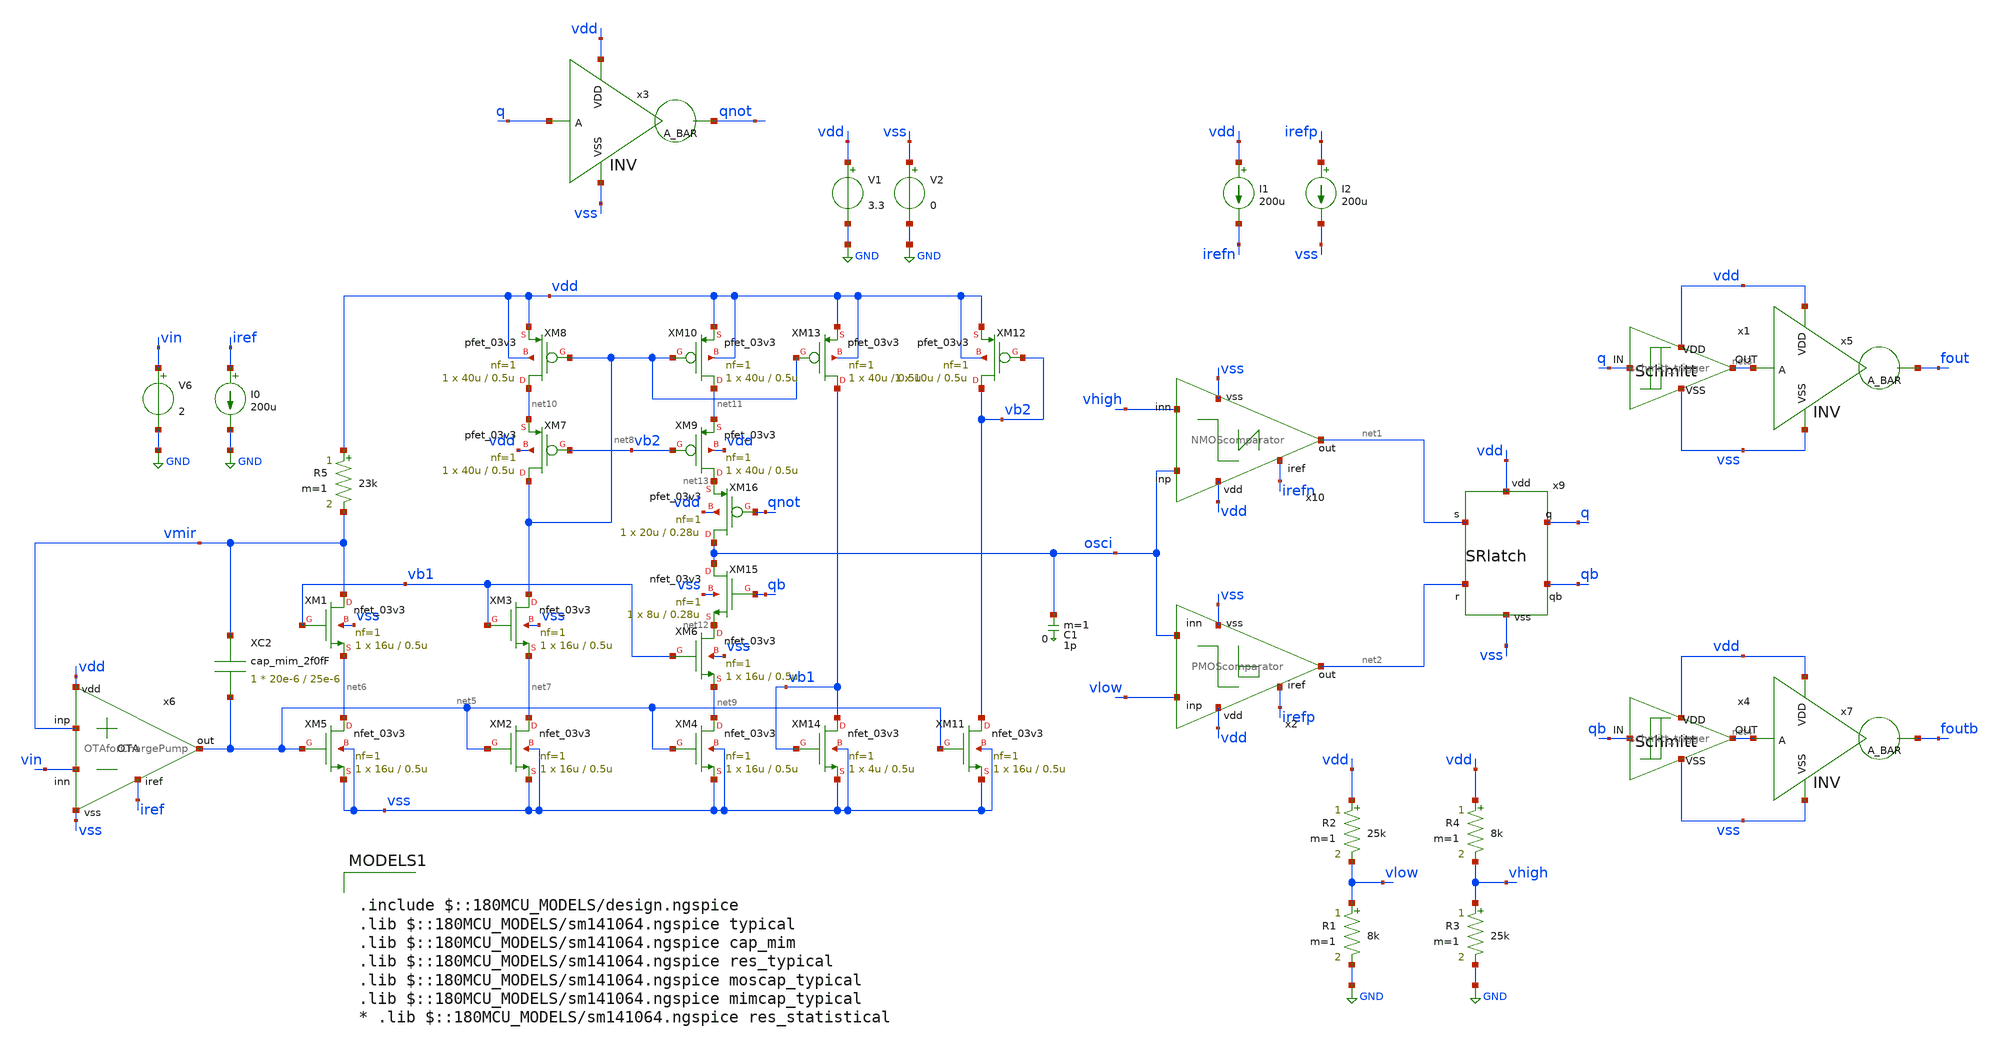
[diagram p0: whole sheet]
** sch_path: designs/libs/qw_core_analog/RVCO_0812/RVCO_0812.sch
**.subckt RVCO_0812
V1 vdd GND 3.3
V2 vss GND 0
C1 osci 0 1p m=1
I1 vdd irefn 200u
I2 irefp vss 200u
R1 vlow GND 8k m=1
R2 vdd vlow 25k m=1
R3 vhigh GND 25k m=1
R4 vdd vhigh 8k m=1
x9 vdd net1 q qb net2 vss SRlatch
x2 vdd irefp vlow net2 osci vss PMOScomparator
x10 vdd osci net1 vhigh irefn vss NMOScomparator
x3 vdd q qnot vss INV
x1 q net3 vdd vss schmitt_trigger
x4 qb net4 vdd vss schmitt_trigger
x5 vdd net3 fout vss INV
x7 vdd net4 foutb vss INV
x6 vdd iref vmir vin net5 vss OTAforChargePump
XM5 net6 net5 vss vss nfet_03v3 L=0.5u W=16u nf=1 ad='int((nf+1)/2) * W/nf * 0.18u' as='int((nf+2)/2) * W/nf * 0.18u'
+ pd='2*int((nf+1)/2) * (W/nf + 0.18u)' ps='2*int((nf+2)/2) * (W/nf + 0.18u)' nrd='0.18u / W' nrs='0.18u / W'
+ sa=0 sb=0 sd=0 m=1
XM1 vmir vb1 net6 vss nfet_03v3 L=0.5u W=16u nf=1 ad='int((nf+1)/2) * W/nf * 0.18u' as='int((nf+2)/2) * W/nf * 0.18u'
+ pd='2*int((nf+1)/2) * (W/nf + 0.18u)' ps='2*int((nf+2)/2) * (W/nf + 0.18u)' nrd='0.18u / W' nrs='0.18u / W'
+ sa=0 sb=0 sd=0 m=1
XM2 net7 net5 vss vss nfet_03v3 L=0.5u W=16u nf=1 ad='int((nf+1)/2) * W/nf * 0.18u' as='int((nf+2)/2) * W/nf * 0.18u'
+ pd='2*int((nf+1)/2) * (W/nf + 0.18u)' ps='2*int((nf+2)/2) * (W/nf + 0.18u)' nrd='0.18u / W' nrs='0.18u / W'
+ sa=0 sb=0 sd=0 m=1
XM3 net8 vb1 net7 vss nfet_03v3 L=0.5u W=16u nf=1 ad='int((nf+1)/2) * W/nf * 0.18u' as='int((nf+2)/2) * W/nf * 0.18u'
+ pd='2*int((nf+1)/2) * (W/nf + 0.18u)' ps='2*int((nf+2)/2) * (W/nf + 0.18u)' nrd='0.18u / W' nrs='0.18u / W'
+ sa=0 sb=0 sd=0 m=1
XM4 net9 net5 vss vss nfet_03v3 L=0.5u W=16u nf=1 ad='int((nf+1)/2) * W/nf * 0.18u' as='int((nf+2)/2) * W/nf * 0.18u'
+ pd='2*int((nf+1)/2) * (W/nf + 0.18u)' ps='2*int((nf+2)/2) * (W/nf + 0.18u)' nrd='0.18u / W' nrs='0.18u / W'
+ sa=0 sb=0 sd=0 m=1
XM6 net12 vb1 net9 vss nfet_03v3 L=0.5u W=16u nf=1 ad='int((nf+1)/2) * W/nf * 0.18u' as='int((nf+2)/2) * W/nf * 0.18u'
+ pd='2*int((nf+1)/2) * (W/nf + 0.18u)' ps='2*int((nf+2)/2) * (W/nf + 0.18u)' nrd='0.18u / W' nrs='0.18u / W'
+ sa=0 sb=0 sd=0 m=1
XM7 net8 vb2 net10 vdd pfet_03v3 L=0.5u W=40u nf=1 ad='int((nf+1)/2) * W/nf * 0.18u' as='int((nf+2)/2) * W/nf * 0.18u'
+ pd='2*int((nf+1)/2) * (W/nf + 0.18u)' ps='2*int((nf+2)/2) * (W/nf + 0.18u)' nrd='0.18u / W' nrs='0.18u / W'
+ sa=0 sb=0 sd=0 m=1
XM8 net10 net8 vdd vdd pfet_03v3 L=0.5u W=40u nf=1 ad='int((nf+1)/2) * W/nf * 0.18u' as='int((nf+2)/2) * W/nf * 0.18u'
+ pd='2*int((nf+1)/2) * (W/nf + 0.18u)' ps='2*int((nf+2)/2) * (W/nf + 0.18u)' nrd='0.18u / W' nrs='0.18u / W'
+ sa=0 sb=0 sd=0 m=1
XM9 net13 vb2 net11 vdd pfet_03v3 L=0.5u W=40u nf=1 ad='int((nf+1)/2) * W/nf * 0.18u' as='int((nf+2)/2) * W/nf * 0.18u'
+ pd='2*int((nf+1)/2) * (W/nf + 0.18u)' ps='2*int((nf+2)/2) * (W/nf + 0.18u)' nrd='0.18u / W' nrs='0.18u / W'
+ sa=0 sb=0 sd=0 m=1
XM10 net11 net8 vdd vdd pfet_03v3 L=0.5u W=40u nf=1 ad='int((nf+1)/2) * W/nf * 0.18u' as='int((nf+2)/2) * W/nf * 0.18u'
+ pd='2*int((nf+1)/2) * (W/nf + 0.18u)' ps='2*int((nf+2)/2) * (W/nf + 0.18u)' nrd='0.18u / W' nrs='0.18u / W'
+ sa=0 sb=0 sd=0 m=1
R5 vdd vmir 23k m=1
XM11 vb2 net5 vss vss nfet_03v3 L=0.5u W=16u nf=1 ad='int((nf+1)/2) * W/nf * 0.18u' as='int((nf+2)/2) * W/nf * 0.18u'
+ pd='2*int((nf+1)/2) * (W/nf + 0.18u)' ps='2*int((nf+2)/2) * (W/nf + 0.18u)' nrd='0.18u / W' nrs='0.18u / W'
+ sa=0 sb=0 sd=0 m=1
XM12 vb2 vb2 vdd vdd pfet_03v3 L=0.5u W=10u nf=1 ad='int((nf+1)/2) * W/nf * 0.18u' as='int((nf+2)/2) * W/nf * 0.18u'
+ pd='2*int((nf+1)/2) * (W/nf + 0.18u)' ps='2*int((nf+2)/2) * (W/nf + 0.18u)' nrd='0.18u / W' nrs='0.18u / W'
+ sa=0 sb=0 sd=0 m=1
XM13 vb1 net8 vdd vdd pfet_03v3 L=0.5u W=40u nf=1 ad='int((nf+1)/2) * W/nf * 0.18u' as='int((nf+2)/2) * W/nf * 0.18u'
+ pd='2*int((nf+1)/2) * (W/nf + 0.18u)' ps='2*int((nf+2)/2) * (W/nf + 0.18u)' nrd='0.18u / W' nrs='0.18u / W'
+ sa=0 sb=0 sd=0 m=1
XM14 vb1 vb1 vss vss nfet_03v3 L=0.5u W=4u nf=1 ad='int((nf+1)/2) * W/nf * 0.18u' as='int((nf+2)/2) * W/nf * 0.18u'
+ pd='2*int((nf+1)/2) * (W/nf + 0.18u)' ps='2*int((nf+2)/2) * (W/nf + 0.18u)' nrd='0.18u / W' nrs='0.18u / W'
+ sa=0 sb=0 sd=0 m=1
XM15 osci qb net12 vss nfet_03v3 L=0.28u W=8u nf=1 ad='int((nf+1)/2) * W/nf * 0.18u' as='int((nf+2)/2) * W/nf * 0.18u'
+ pd='2*int((nf+1)/2) * (W/nf + 0.18u)' ps='2*int((nf+2)/2) * (W/nf + 0.18u)' nrd='0.18u / W' nrs='0.18u / W'
+ sa=0 sb=0 sd=0 m=1
XM16 osci qnot net13 vdd pfet_03v3 L=0.28u W=20u nf=1 ad='int((nf+1)/2) * W/nf * 0.18u' as='int((nf+2)/2) * W/nf * 0.18u'
+ pd='2*int((nf+1)/2) * (W/nf + 0.18u)' ps='2*int((nf+2)/2) * (W/nf + 0.18u)' nrd='0.18u / W' nrs='0.18u / W'
+ sa=0 sb=0 sd=0 m=1
V6 vin GND 2
I0 iref GND 200u
XC2 vmir net5 cap_mim_2f0fF c_width=20e-6 c_length=25e-6 m=1
**** begin user architecture code

.include $::180MCU_MODELS/design.ngspice
.lib $::180MCU_MODELS/sm141064.ngspice typical



.param par_vth=0 par_k=0 par_l=0 par_w=0 par_leff=0 par_weff=0 p_sqrtarea=0 var_k=0 var_vth=0
.control
save all

**OP
**show all > op.log
**show all

** Source settings
**alter @V5[PULSE] = [ 1.64 1.66 20n 0.1n 0.1n 19.98n 40n 0 ]
**alter @V4[PULSE] = [ 1.66 1.64 20n 0.1n 0.1n 19.98n 40n 0 ]
**alter @V3[PULSE] = [ 0 3.3 10n 0.01n 0.01n 9.98n 20n 0 ]
**alter @V4[PULSE] = [ 0 3.3 50u 0.1u 0.1u 49.8u 100u 0 ]
alter @V1[PULSE] = [ 0 3.3 5n 1n 1n 49.998u 100u 0 ]

** Simulation settings

tran 1n 100u

write RVCO_0812.raw
.endc



.include $::180MCU_MODELS/design.ngspice
.lib $::180MCU_MODELS/sm141064.ngspice typical
.lib $::180MCU_MODELS/sm141064.ngspice cap_mim
.lib $::180MCU_MODELS/sm141064.ngspice res_typical
.lib $::180MCU_MODELS/sm141064.ngspice moscap_typical
.lib $::180MCU_MODELS/sm141064.ngspice mimcap_typical
* .lib $::180MCU_MODELS/sm141064.ngspice res_statistical

**** end user architecture code
**.ends
.GLOBAL GND
.end
